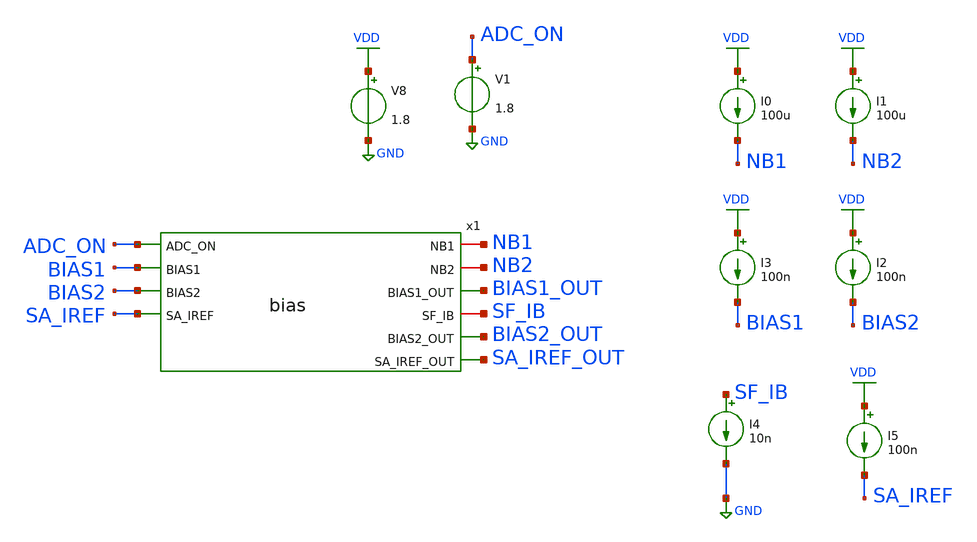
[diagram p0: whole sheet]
** sch_path: xschem/testbench/bias_tb.sch
**.subckt bias_tb
x1 NB1 ADC_ON NB2 BIAS1 BIAS1_OUT SF_IB BIAS2 BIAS2_OUT SA_IREF SA_IREF_OUT bias
V8 VDD GND 1.8
V1 ADC_ON GND 1.8
I0 VDD NB1 100u
I1 VDD NB2 100u
I2 VDD BIAS2 100n
I3 VDD BIAS1 100n
I4 SF_IB GND 10n
I5 VDD SA_IREF 100n
**** begin user architecture code

** opencircuitdesign pdks install
.lib $::SKYWATER_MODELS/sky130.lib.spice tt


**** end user architecture code
**.ends
.GLOBAL GND
.GLOBAL VDD
**** begin user architecture code


.options gmin=10e-20
.control
save all

*dc v2 0 1.8 0.05
*plot v(test)
tran 1u 200u
.endc


**** end user architecture code
.end
